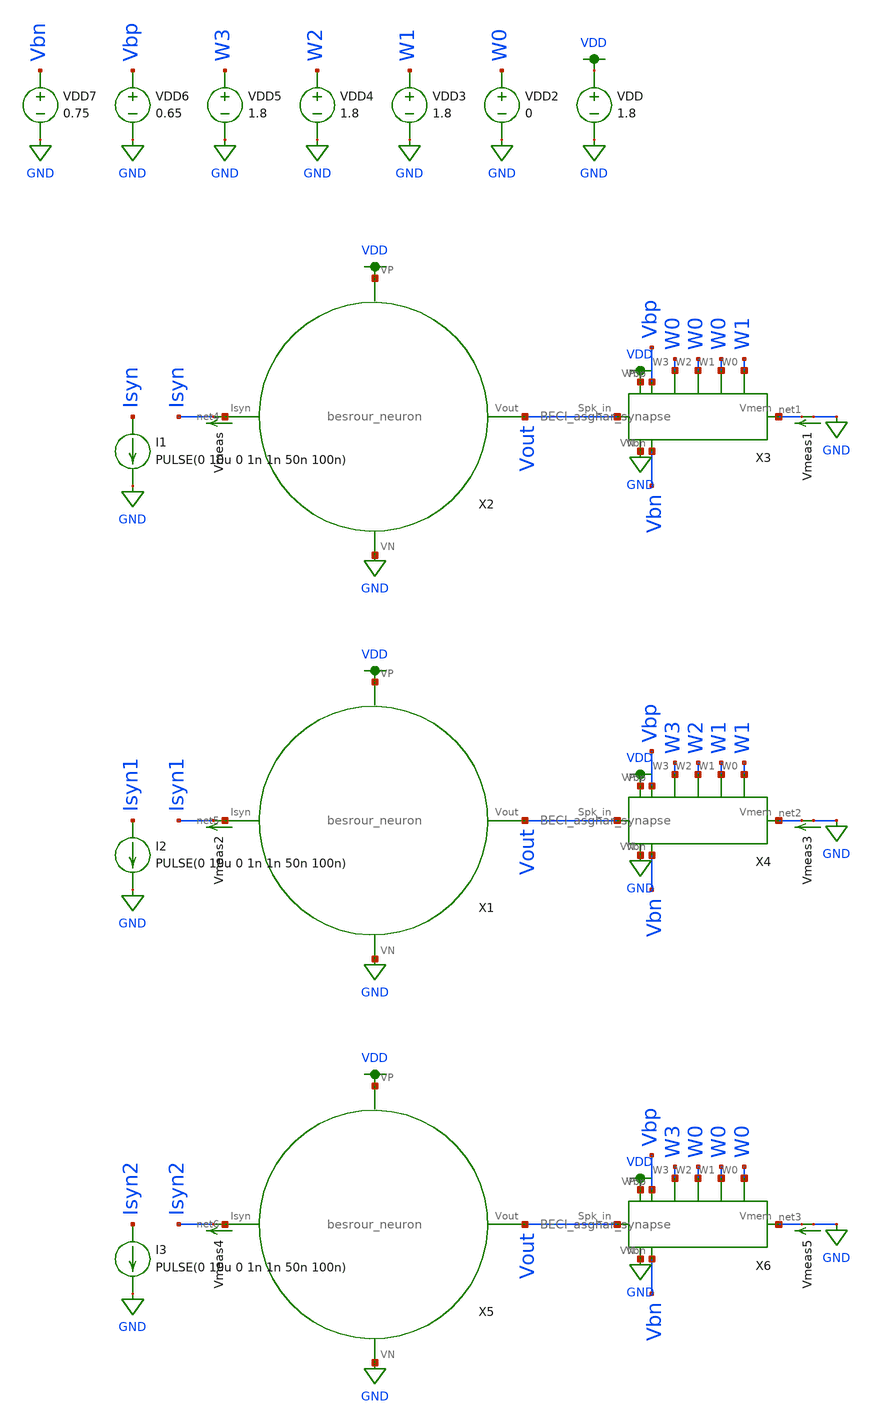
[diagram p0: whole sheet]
** sch_path: schematic/tran_neuron.sch
**.subckt tran_neuron
VDD VDD GND 1.8
I1 Isyn GND PULSE(0 10u 0 1n 1n 50n 100n)
Vmeas net4 Isyn 0
.save i(vmeas)
VDD2 W0 GND 0
VDD3 W1 GND 1.8
VDD4 W2 GND 1.8
VDD5 W3 GND 1.8
VDD6 Vbp GND 0.65
VDD7 Vbn GND 0.75
X2 net4 Vout VDD GND besrour_neuron
X3 VDD GND Vout net1 W0 W0 W0 W1 Vbp Vbn BECI_asghar_synapse
Vmeas1 GND net1 0
.save i(vmeas1)
I2 Isyn1 GND PULSE(0 10u 0 1n 1n 50n 100n)
Vmeas2 net5 Isyn1 0
.save i(vmeas2)
X1 net5 Vout VDD GND besrour_neuron
X4 VDD GND Vout net2 W3 W2 W1 W1 Vbp Vbn BECI_asghar_synapse
Vmeas3 GND net2 0
.save i(vmeas3)
I3 Isyn2 GND PULSE(0 10u 0 1n 1n 50n 100n)
Vmeas4 net6 Isyn2 0
.save i(vmeas4)
X5 net6 Vout VDD GND besrour_neuron
X6 VDD GND Vout net3 W3 W0 W0 W0 Vbp Vbn BECI_asghar_synapse
Vmeas5 GND net3 0
.save i(vmeas5)
**** begin user architecture code

.param W=12
.param L=0.5
.tran 0.1n 250n
.save all


.option wnflag=1
.param MC_SWITCH=0.0
.lib ~/skywater/skywater-pdk/libraries/sky130_fd_pr_ngspice/latest/models/sky130.lib.spice tt

**** end user architecture code
**.ends
.GLOBAL GND
.GLOBAL VDD
.end
